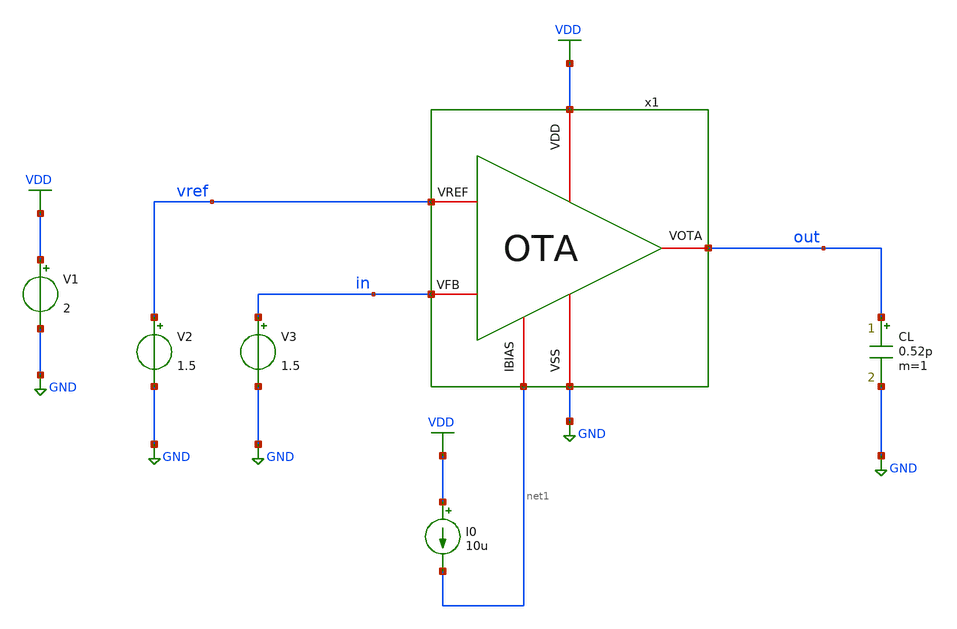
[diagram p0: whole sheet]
** sch_path: designs/libs/tb_ldo/tb_ldo/tb_ldo_OTA/tb_ldo_OTA_dc/tb_ldo_OTA_dc.sch
**.subckt tb_ldo_OTA_dc
V1 VDD GND 2
V2 vref GND 1.5
I0 VDD net1 10u
CL out GND 0.52p m=1
V3 in GND 1.5
x1 VDD vref in out net1 GND OTA
**** begin user architecture code

.include $::180MCU_MODELS/design.ngspice
.lib $::180MCU_MODELS/sm141064.ngspice typical
.lib $::180MCU_MODELS/sm141064.ngspice cap_mim
.lib $::180MCU_MODELS/sm141064.ngspice moscap_typical
.lib $::180MCU_MODELS/sm141064.ngspice mimcap_typical
.lib $::180MCU_MODELS/sm141064.ngspice res_typical
* .lib $::180MCU_MODELS/sm141064.ngspice res_statistical
* ngspice commands




.control
save all

** Voltage offset simulation
dc V3 1.4 1.6 0.001

** Measurements
let vtarget = v(vdd)/2
let vin = v(in)
let vout = v(out)
meas dc offset FIND vin WHEN vout=vtarget RISE=1
let vos = 1.5 - offset
print vos

** Plots
setplot dc1
plot vout

write tb_ldo_OTA_dc1.raw

** VDD DC sweep simulation
dc V1 0 5 0.1

** Plots
setplot dc2
let vout = v(out)
plot vout

write tb_ldo_OTA_dc2.raw

.endc
* ngspice commands



**** end user architecture code
**.ends

* expanding   symbol:  libs/core_ldo/ldo/ldo_OTA/OTA.sym # of pins=6
** sym_path: designs/libs/core_ldo/ldo/OTA.sym
** sch_path: designs/libs/core_ldo/ldo/OTA.sch
.subckt OTA VDD VREF VFB VOTA IBIAS VSS
*.iopin VDD
*.iopin VSS
*.iopin VOTA
*.iopin VREF
*.iopin IBIAS
*.iopin VFB
XM3 net2 net2 VDD VDD pfet_05v0 L=2.00u W=8.00u nf=1 ad='int((nf+1)/2) * W/nf * 0.18u' as='int((nf+2)/2) * W/nf * 0.18u'
+ pd='2*int((nf+1)/2) * (W/nf + 0.18u)' ps='2*int((nf+2)/2) * (W/nf + 0.18u)' nrd='0.18u / W' nrs='0.18u / W'
+ sa=0 sb=0 sd=0 m=1
XM4 net3 net3 VDD VDD pfet_05v0 L=2.00u W=8.00u nf=1 ad='int((nf+1)/2) * W/nf * 0.18u' as='int((nf+2)/2) * W/nf * 0.18u'
+ pd='2*int((nf+1)/2) * (W/nf + 0.18u)' ps='2*int((nf+2)/2) * (W/nf + 0.18u)' nrd='0.18u / W' nrs='0.18u / W'
+ sa=0 sb=0 sd=0 m=1
XM5 net4 net2 VDD VDD pfet_05v0 L=2.00u W=8.00u nf=1 ad='int((nf+1)/2) * W/nf * 0.18u' as='int((nf+2)/2) * W/nf * 0.18u'
+ pd='2*int((nf+1)/2) * (W/nf + 0.18u)' ps='2*int((nf+2)/2) * (W/nf + 0.18u)' nrd='0.18u / W' nrs='0.18u / W'
+ sa=0 sb=0 sd=0 m=1
XM6 VOTA net3 VDD VDD pfet_05v0 L=2.00u W=8.00u nf=1 ad='int((nf+1)/2) * W/nf * 0.18u' as='int((nf+2)/2) * W/nf * 0.18u'
+ pd='2*int((nf+1)/2) * (W/nf + 0.18u)' ps='2*int((nf+2)/2) * (W/nf + 0.18u)' nrd='0.18u / W' nrs='0.18u / W'
+ sa=0 sb=0 sd=0 m=2
XM9 IBIAS IBIAS VSS VSS nfet_05v0 L=2.00u W=4.00u nf=1 ad='int((nf+1)/2) * W/nf * 0.18u' as='int((nf+2)/2) * W/nf * 0.18u'
+ pd='2*int((nf+1)/2) * (W/nf + 0.18u)' ps='2*int((nf+2)/2) * (W/nf + 0.18u)' nrd='0.18u / W' nrs='0.18u / W'
+ sa=0 sb=0 sd=0 m=1
XM10 net1 IBIAS VSS VSS nfet_05v0 L=2.00u W=4.00u nf=1 ad='int((nf+1)/2) * W/nf * 0.18u' as='int((nf+2)/2) * W/nf * 0.18u'
+ pd='2*int((nf+1)/2) * (W/nf + 0.18u)' ps='2*int((nf+2)/2) * (W/nf + 0.18u)' nrd='0.18u / W' nrs='0.18u / W'
+ sa=0 sb=0 sd=0 m=1
XM7 net4 net4 VSS VSS nfet_05v0 L=2.00u W=4.00u nf=1 ad='int((nf+1)/2) * W/nf * 0.18u' as='int((nf+2)/2) * W/nf * 0.18u'
+ pd='2*int((nf+1)/2) * (W/nf + 0.18u)' ps='2*int((nf+2)/2) * (W/nf + 0.18u)' nrd='0.18u / W' nrs='0.18u / W'
+ sa=0 sb=0 sd=0 m=1
XM8 VOTA net4 VSS VSS nfet_05v0 L=2.00u W=4.00u nf=1 ad='int((nf+1)/2) * W/nf * 0.18u' as='int((nf+2)/2) * W/nf * 0.18u'
+ pd='2*int((nf+1)/2) * (W/nf + 0.18u)' ps='2*int((nf+2)/2) * (W/nf + 0.18u)' nrd='0.18u / W' nrs='0.18u / W'
+ sa=0 sb=0 sd=0 m=2
XM1 net2 VREF net1 net1 nfet_05v0 L=0.60u W=40.00u nf=1 ad='int((nf+1)/2) * W/nf * 0.18u' as='int((nf+2)/2) * W/nf * 0.18u'
+ pd='2*int((nf+1)/2) * (W/nf + 0.18u)' ps='2*int((nf+2)/2) * (W/nf + 0.18u)' nrd='0.18u / W' nrs='0.18u / W'
+ sa=0 sb=0 sd=0 m=1
XM2 net3 VFB net1 net1 nfet_05v0 L=0.60u W=40.00u nf=1 ad='int((nf+1)/2) * W/nf * 0.18u' as='int((nf+2)/2) * W/nf * 0.18u'
+ pd='2*int((nf+1)/2) * (W/nf + 0.18u)' ps='2*int((nf+2)/2) * (W/nf + 0.18u)' nrd='0.18u / W' nrs='0.18u / W'
+ sa=0 sb=0 sd=0 m=1
.ends

.GLOBAL GND
.GLOBAL VDD
.end
